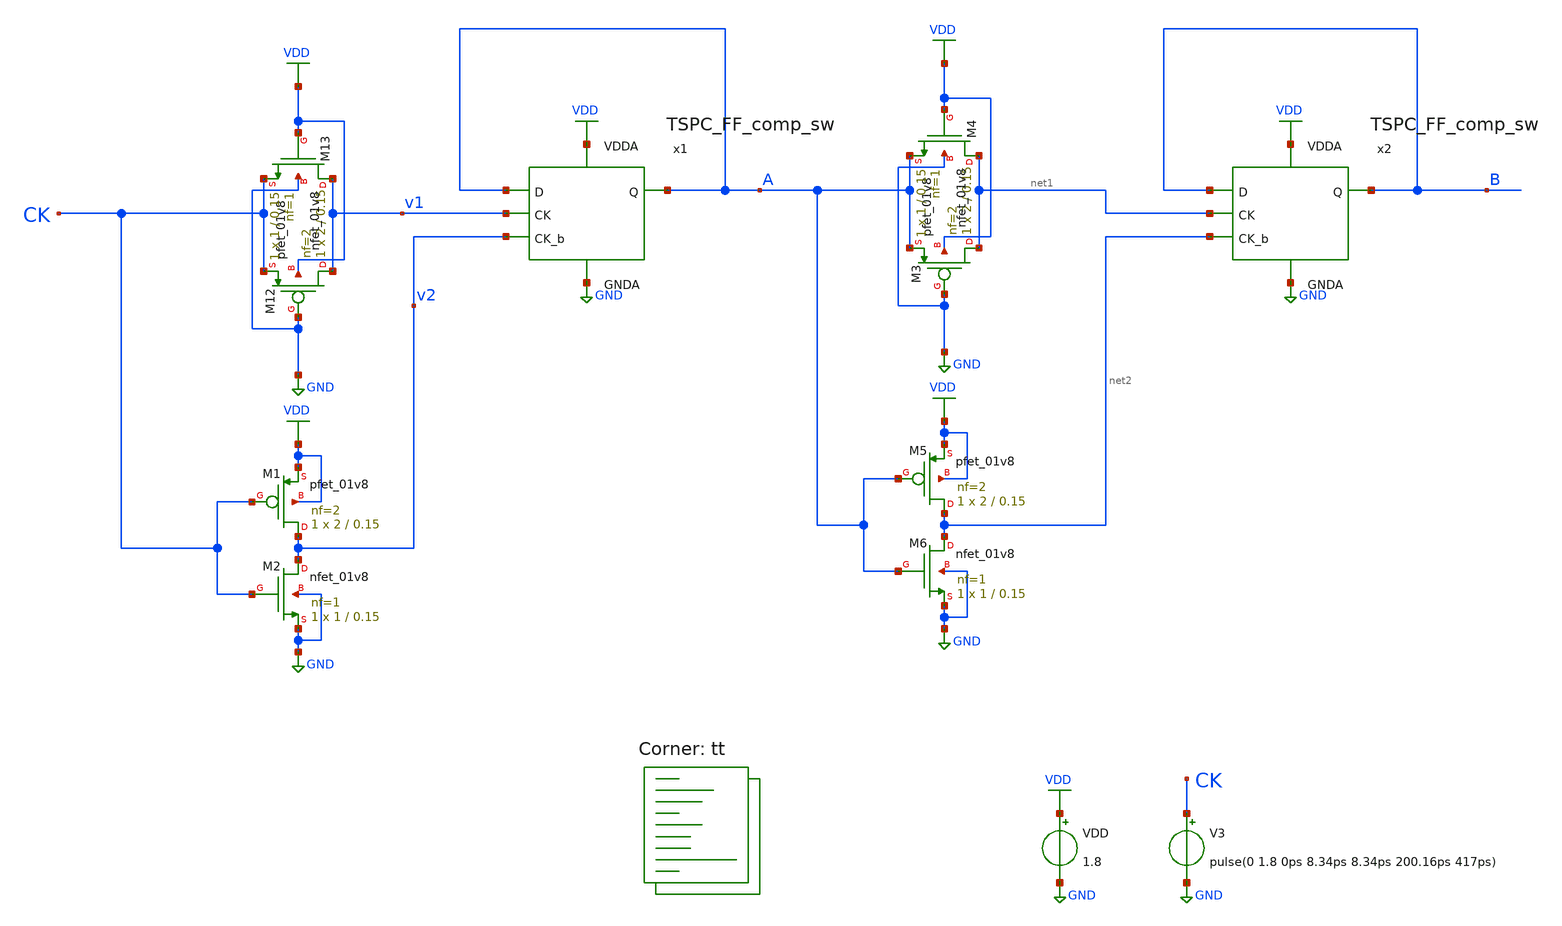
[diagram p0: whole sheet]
** sch_path: projects/pll/divider/xschem_ngspice/tb_TSPC_FF_comp_sw.sch
**.subckt tb_TSPC_FF_comp_sw
VDD VDD GND 1.8
V3 CK GND pulse(0 1.8 0ps 8.34ps 8.34ps 200.16ps 417ps)
x1 VDD A A v2 GND v1 TSPC_FF_comp_sw
XM12 v1 GND CK VDD sky130_fd_pr__pfet_01v8 L=0.15 W=2 nf=2 ad='int((nf+1)/2) * W/nf * 0.29' as='int((nf+2)/2) * W/nf * 0.29'
+ pd='2*int((nf+1)/2) * (W/nf + 0.29)' ps='2*int((nf+2)/2) * (W/nf + 0.29)' nrd='0.29 / W' nrs='0.29 / W'
+ sa=0 sb=0 sd=0 mult=1 m=1
XM13 v1 VDD CK GND sky130_fd_pr__nfet_01v8 L=0.15 W=1 nf=1 ad='int((nf+1)/2) * W/nf * 0.29' as='int((nf+2)/2) * W/nf * 0.29'
+ pd='2*int((nf+1)/2) * (W/nf + 0.29)' ps='2*int((nf+2)/2) * (W/nf + 0.29)' nrd='0.29 / W' nrs='0.29 / W'
+ sa=0 sb=0 sd=0 mult=1 m=1
XM1 v2 CK VDD VDD sky130_fd_pr__pfet_01v8 L=0.15 W=2 nf=2 ad='int((nf+1)/2) * W/nf * 0.29' as='int((nf+2)/2) * W/nf * 0.29'
+ pd='2*int((nf+1)/2) * (W/nf + 0.29)' ps='2*int((nf+2)/2) * (W/nf + 0.29)' nrd='0.29 / W' nrs='0.29 / W'
+ sa=0 sb=0 sd=0 mult=1 m=1
XM2 v2 CK GND GND sky130_fd_pr__nfet_01v8 L=0.15 W=1 nf=1 ad='int((nf+1)/2) * W/nf * 0.29' as='int((nf+2)/2) * W/nf * 0.29'
+ pd='2*int((nf+1)/2) * (W/nf + 0.29)' ps='2*int((nf+2)/2) * (W/nf + 0.29)' nrd='0.29 / W' nrs='0.29 / W'
+ sa=0 sb=0 sd=0 mult=1 m=1
x2 VDD B B net2 GND net1 TSPC_FF_comp_sw
XM3 net1 GND A VDD sky130_fd_pr__pfet_01v8 L=0.15 W=2 nf=2 ad='int((nf+1)/2) * W/nf * 0.29' as='int((nf+2)/2) * W/nf * 0.29'
+ pd='2*int((nf+1)/2) * (W/nf + 0.29)' ps='2*int((nf+2)/2) * (W/nf + 0.29)' nrd='0.29 / W' nrs='0.29 / W'
+ sa=0 sb=0 sd=0 mult=1 m=1
XM4 net1 VDD A GND sky130_fd_pr__nfet_01v8 L=0.15 W=1 nf=1 ad='int((nf+1)/2) * W/nf * 0.29' as='int((nf+2)/2) * W/nf * 0.29'
+ pd='2*int((nf+1)/2) * (W/nf + 0.29)' ps='2*int((nf+2)/2) * (W/nf + 0.29)' nrd='0.29 / W' nrs='0.29 / W'
+ sa=0 sb=0 sd=0 mult=1 m=1
XM5 net2 A VDD VDD sky130_fd_pr__pfet_01v8 L=0.15 W=2 nf=2 ad='int((nf+1)/2) * W/nf * 0.29' as='int((nf+2)/2) * W/nf * 0.29'
+ pd='2*int((nf+1)/2) * (W/nf + 0.29)' ps='2*int((nf+2)/2) * (W/nf + 0.29)' nrd='0.29 / W' nrs='0.29 / W'
+ sa=0 sb=0 sd=0 mult=1 m=1
XM6 net2 A GND GND sky130_fd_pr__nfet_01v8 L=0.15 W=1 nf=1 ad='int((nf+1)/2) * W/nf * 0.29' as='int((nf+2)/2) * W/nf * 0.29'
+ pd='2*int((nf+1)/2) * (W/nf + 0.29)' ps='2*int((nf+2)/2) * (W/nf + 0.29)' nrd='0.29 / W' nrs='0.29 / W'
+ sa=0 sb=0 sd=0 mult=1 m=1
**** begin user architecture code



.include /foss/pdks/sky130A/libs.ref/sky130_fd_sc_hd/spice/sky130_fd_sc_hd.spice

.option method=gear
.option wnflag=1
* .option savecurrents

.save @m.x1.xm1.msky130_fd_pr__pfet_01v8[gm] @m.x1.xm2.msky130_fd_pr__nfet_01v8[gm] @m.x1.xm3.msky130_fd_pr__pfet_01v8[gm] @m.x1.xm4.msky130_fd_pr__nfet_01v8[gm] @m.x1.xm5.msky130_fd_pr__pfet_01v8[gm] @m.x1.xm6.msky130_fd_pr__nfet_01v8[gm] @m.x1.xm7.msky130_fd_pr__nfet_01v8[gm]
 @m.x2.xm1.msky130_fd_pr__pfet_01v8[gm] @m.x1.xm2.msky130_fd_pr__nfet_01v8[gm]
+ @m.x2.xm3.msky130_fd_pr__pfet_01v8[gm] @m.x2.xm4.msky130_fd_pr__nfet_01v8[gm] @m.x2.xm5.msky130_fd_pr__pfet_01v8[gm]
+ @m.x2.xm6.msky130_fd_pr__nfet_01v8[gm] @m.x2.xm7.msky130_fd_pr__nfet_01v8[gm]
 @v.x1.vmeas @v.x1.vmeas1 @v.x1.vmeas2 @v.x2.vmeas @v.x2.vmeas1 @v.x2.vmeas2


.control

  * save v(a) v(b) v(v1) v(v2) v(ck) v(ck_b)
  save all
  *tran 0.1n 1u
  tran 0.2p 10n
  remzerovec
  write tb_TSPC_FF_comp_sw.raw
  set appendwrite

.endc



.lib $::SKYWATER_MODELS/sky130.lib.spice tt
**** end user architecture code
**.ends

* expanding   symbol:
*+  /foss/designs/my_design/projects/pll/divider/xschem_ngspice/TSPC_FF_comp_sw.sym # of pins=6
** sym_path: projects/pll/divider/xschem_ngspice/TSPC_FF_comp_sw.sym
** sch_path: projects/pll/divider/xschem_ngspice/TSPC_FF_comp_sw.sch
.subckt TSPC_FF_comp_sw VDDA Q D CK_b GNDA CK
*.ipin CK
*.ipin D
*.opin Q
*.ipin VDDA
*.ipin GNDA
*.ipin CK_b
XM1 Q B1 VDDA VDDA sky130_fd_pr__pfet_01v8 L=0.15 W=1 nf=1 ad='int((nf+1)/2) * W/nf * 0.29' as='int((nf+2)/2) * W/nf * 0.29'
+ pd='2*int((nf+1)/2) * (W/nf + 0.29)' ps='2*int((nf+2)/2) * (W/nf + 0.29)' nrd='0.29 / W' nrs='0.29 / W'
+ sa=0 sb=0 sd=0 mult=1 m=1
XM4 net1 CK B2 GNDA sky130_fd_pr__nfet_01v8 L=0.15 W=1 nf=1 ad='int((nf+1)/2) * W/nf * 0.29' as='int((nf+2)/2) * W/nf * 0.29'
+ pd='2*int((nf+1)/2) * (W/nf + 0.29)' ps='2*int((nf+2)/2) * (W/nf + 0.29)' nrd='0.29 / W' nrs='0.29 / W'
+ sa=0 sb=0 sd=0 mult=1 m=1
Vmeas Q net2 0
.save i(vmeas)
XM2 net2 B2 GNDA GNDA sky130_fd_pr__nfet_01v8 L=0.15 W=1 nf=1 ad='int((nf+1)/2) * W/nf * 0.29' as='int((nf+2)/2) * W/nf * 0.29'
+ pd='2*int((nf+1)/2) * (W/nf + 0.29)' ps='2*int((nf+2)/2) * (W/nf + 0.29)' nrd='0.29 / W' nrs='0.29 / W'
+ sa=0 sb=0 sd=0 mult=1 m=1
XM3 B1 A1 VDDA VDDA sky130_fd_pr__pfet_01v8 L=0.15 W=1 nf=1 ad='int((nf+1)/2) * W/nf * 0.29' as='int((nf+2)/2) * W/nf * 0.29'
+ pd='2*int((nf+1)/2) * (W/nf + 0.29)' ps='2*int((nf+2)/2) * (W/nf + 0.29)' nrd='0.29 / W' nrs='0.29 / W'
+ sa=0 sb=0 sd=0 mult=1 m=1
XM5 B2 A2 GNDA GNDA sky130_fd_pr__nfet_01v8 L=0.15 W=1 nf=1 ad='int((nf+1)/2) * W/nf * 0.29' as='int((nf+2)/2) * W/nf * 0.29'
+ pd='2*int((nf+1)/2) * (W/nf + 0.29)' ps='2*int((nf+2)/2) * (W/nf + 0.29)' nrd='0.29 / W' nrs='0.29 / W'
+ sa=0 sb=0 sd=0 mult=1 m=1
Vmeas1 B1 net1 0
.save i(vmeas1)
XM6 A1 D VDDA VDDA sky130_fd_pr__pfet_01v8 L=0.15 W=1 nf=1 ad='int((nf+1)/2) * W/nf * 0.29' as='int((nf+2)/2) * W/nf * 0.29'
+ pd='2*int((nf+1)/2) * (W/nf + 0.29)' ps='2*int((nf+2)/2) * (W/nf + 0.29)' nrd='0.29 / W' nrs='0.29 / W'
+ sa=0 sb=0 sd=0 mult=1 m=1
XM8 A2 D GNDA GNDA sky130_fd_pr__nfet_01v8 L=0.15 W=1 nf=1 ad='int((nf+1)/2) * W/nf * 0.29' as='int((nf+2)/2) * W/nf * 0.29'
+ pd='2*int((nf+1)/2) * (W/nf + 0.29)' ps='2*int((nf+2)/2) * (W/nf + 0.29)' nrd='0.29 / W' nrs='0.29 / W'
+ sa=0 sb=0 sd=0 mult=1 m=1
Vmeas2 A1 net3 0
.save i(vmeas2)
XM7 A2 CK net3 VDDA sky130_fd_pr__pfet_01v8 L=0.15 W=1 nf=1 ad='int((nf+1)/2) * W/nf * 0.29' as='int((nf+2)/2) * W/nf * 0.29'
+ pd='2*int((nf+1)/2) * (W/nf + 0.29)' ps='2*int((nf+2)/2) * (W/nf + 0.29)' nrd='0.29 / W' nrs='0.29 / W'
+ sa=0 sb=0 sd=0 mult=1 m=1
XM4_c B2 CK_b net1 VDDA sky130_fd_pr__pfet_01v8 L=0.15 W=1 nf=1 ad='int((nf+1)/2) * W/nf * 0.29' as='int((nf+2)/2) * W/nf * 0.29'
+ pd='2*int((nf+1)/2) * (W/nf + 0.29)' ps='2*int((nf+2)/2) * (W/nf + 0.29)' nrd='0.29 / W' nrs='0.29 / W'
+ sa=0 sb=0 sd=0 mult=1 m=1
XM7_c net3 CK_b A2 GNDA sky130_fd_pr__nfet_01v8 L=0.15 W=1 nf=1 ad='int((nf+1)/2) * W/nf * 0.29' as='int((nf+2)/2) * W/nf * 0.29'
+ pd='2*int((nf+1)/2) * (W/nf + 0.29)' ps='2*int((nf+2)/2) * (W/nf + 0.29)' nrd='0.29 / W' nrs='0.29 / W'
+ sa=0 sb=0 sd=0 mult=1 m=1
.ends

.GLOBAL GND
.GLOBAL VDD
.end
